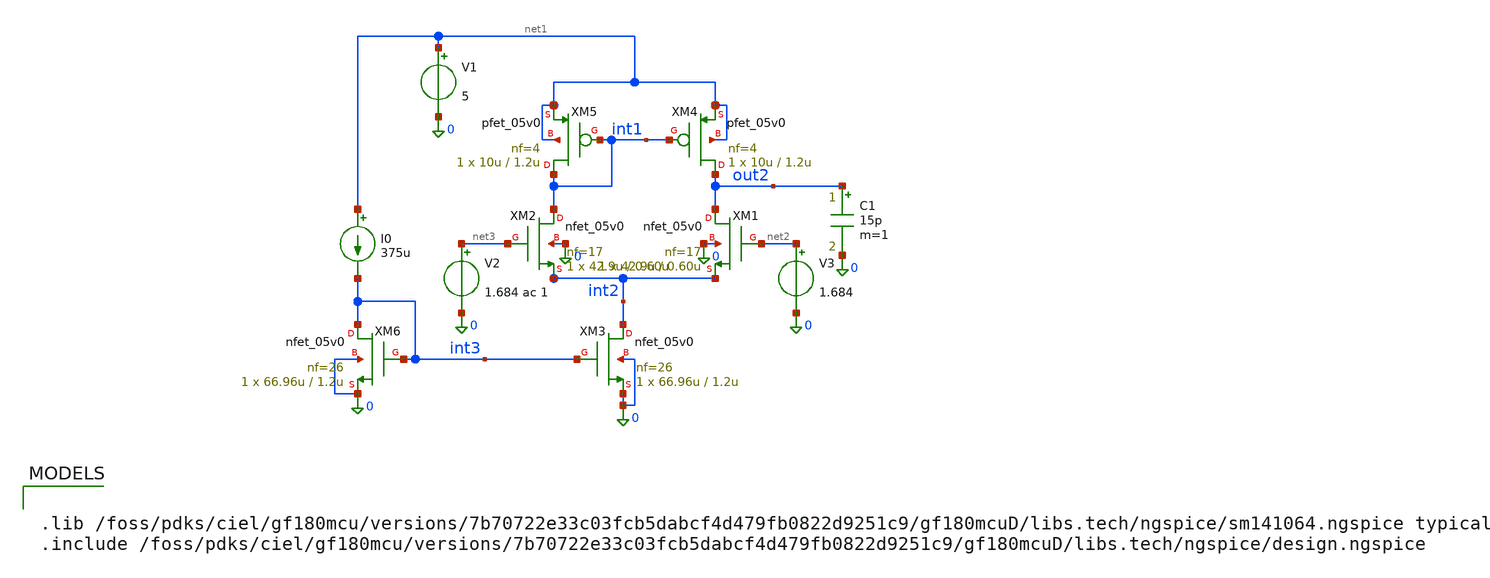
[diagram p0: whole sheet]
** sch_path: RN_Gm3/gm3_ota_old.sch
**.subckt gm3_ota_old
XM1 out2 net2 int2 0 nfet_05v0 L=0.60u W=42.9u nf=17 ad='int((nf+1)/2) * W/nf * 0.18u' as='int((nf+2)/2) * W/nf * 0.18u'
+ pd='2*int((nf+1)/2) * (W/nf + 0.18u)' ps='2*int((nf+2)/2) * (W/nf + 0.18u)' nrd='0.18u / W' nrs='0.18u / W'
+ sa=0 sb=0 sd=0 m=1
XM2 int1 net3 int2 0 nfet_05v0 L=0.60u W=42.9u nf=17 ad='int((nf+1)/2) * W/nf * 0.18u' as='int((nf+2)/2) * W/nf * 0.18u'
+ pd='2*int((nf+1)/2) * (W/nf + 0.18u)' ps='2*int((nf+2)/2) * (W/nf + 0.18u)' nrd='0.18u / W' nrs='0.18u / W'
+ sa=0 sb=0 sd=0 m=1
XM3 int2 int3 0 0 nfet_05v0 L=1.2u W=66.96u nf=26 ad='int((nf+1)/2) * W/nf * 0.18u' as='int((nf+2)/2) * W/nf * 0.18u'
+ pd='2*int((nf+1)/2) * (W/nf + 0.18u)' ps='2*int((nf+2)/2) * (W/nf + 0.18u)' nrd='0.18u / W' nrs='0.18u / W'
+ sa=0 sb=0 sd=0 m=1
XM4 out2 int1 net1 net1 pfet_05v0 L=1.2u W=10u nf=4 ad='int((nf+1)/2) * W/nf * 0.18u' as='int((nf+2)/2) * W/nf * 0.18u'
+ pd='2*int((nf+1)/2) * (W/nf + 0.18u)' ps='2*int((nf+2)/2) * (W/nf + 0.18u)' nrd='0.18u / W' nrs='0.18u / W'
+ sa=0 sb=0 sd=0 m=1
XM5 int1 int1 net1 net1 pfet_05v0 L=1.2u W=10u nf=4 ad='int((nf+1)/2) * W/nf * 0.18u' as='int((nf+2)/2) * W/nf * 0.18u'
+ pd='2*int((nf+1)/2) * (W/nf + 0.18u)' ps='2*int((nf+2)/2) * (W/nf + 0.18u)' nrd='0.18u / W' nrs='0.18u / W'
+ sa=0 sb=0 sd=0 m=1
V1 net1 0 5
V2 net3 0 1.684 ac 1
V3 net2 0 1.684
C1 out2 0 15p m=1
I0 net1 int3 375u
XM6 int3 int3 0 0 nfet_05v0 L=1.2u W=66.96u nf=26 ad='int((nf+1)/2) * W/nf * 0.18u' as='int((nf+2)/2) * W/nf * 0.18u'
+ pd='2*int((nf+1)/2) * (W/nf + 0.18u)' ps='2*int((nf+2)/2) * (W/nf + 0.18u)' nrd='0.18u / W' nrs='0.18u / W'
+ sa=0 sb=0 sd=0 m=1
**** begin user architecture code


.lib /foss/pdks/ciel/gf180mcu/versions/7b70722e33c03fcb5dabcf4d479fb0822d9251c9/gf180mcuD/libs.tech/ngspice/sm141064.ngspice typical
.include /foss/pdks/ciel/gf180mcu/versions/7b70722e33c03fcb5dabcf4d479fb0822d9251c9/gf180mcuD/libs.tech/ngspice/design.ngspice




.control
  	save all
	op
	ac dec 20 1 100Meg
	remzerovec
	write gm3_OTA_ac.raw
.endc

.options savecurrents


**** end user architecture code
**.ends
.end
